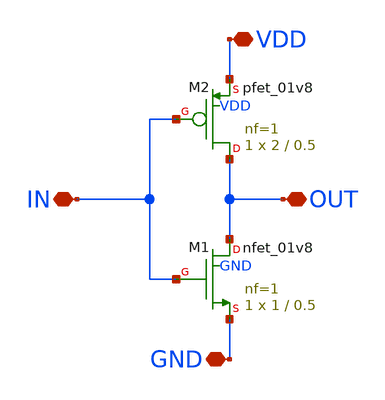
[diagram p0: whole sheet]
** sch_path: design_data/xschem/inv_magic.sch
**.subckt inv_magic OUT VDD IN GND
*.iopin OUT
*.iopin VDD
*.iopin IN
*.iopin GND
XM1 OUT IN GND GND sky130_fd_pr__nfet_01v8 L=0.5 W=1 nf=1 ad='int((1 + 1)/2) * 1 / 1 * 0.29' as='int((1 + 2)/2) * 1 / 1 * 0.29'
+ pd='2*int((1 + 1)/2) * (1 / 1 + 0.29)' ps='2*int((1 + 2)/2) * (1 / 1 + 0.29)' nrd='0.29 / 1 ' nrs='0.29 / 1 '
+ sa=0 sb=0 sd=0 mult=1 m=1
XM2 OUT IN VDD VDD sky130_fd_pr__pfet_01v8 L=0.5 W=2 nf=1 ad='int((1 + 1)/2) * 2 / 1 * 0.29' as='int((1 + 2)/2) * 2 / 1 * 0.29'
+ pd='2*int((1 + 1)/2) * (2 / 1 + 0.29)' ps='2*int((1 + 2)/2) * (2 / 1 + 0.29)' nrd='0.29 / 2 ' nrs='0.29 / 2 '
+ sa=0 sb=0 sd=0 mult=1 m=1
**.ends
.end
